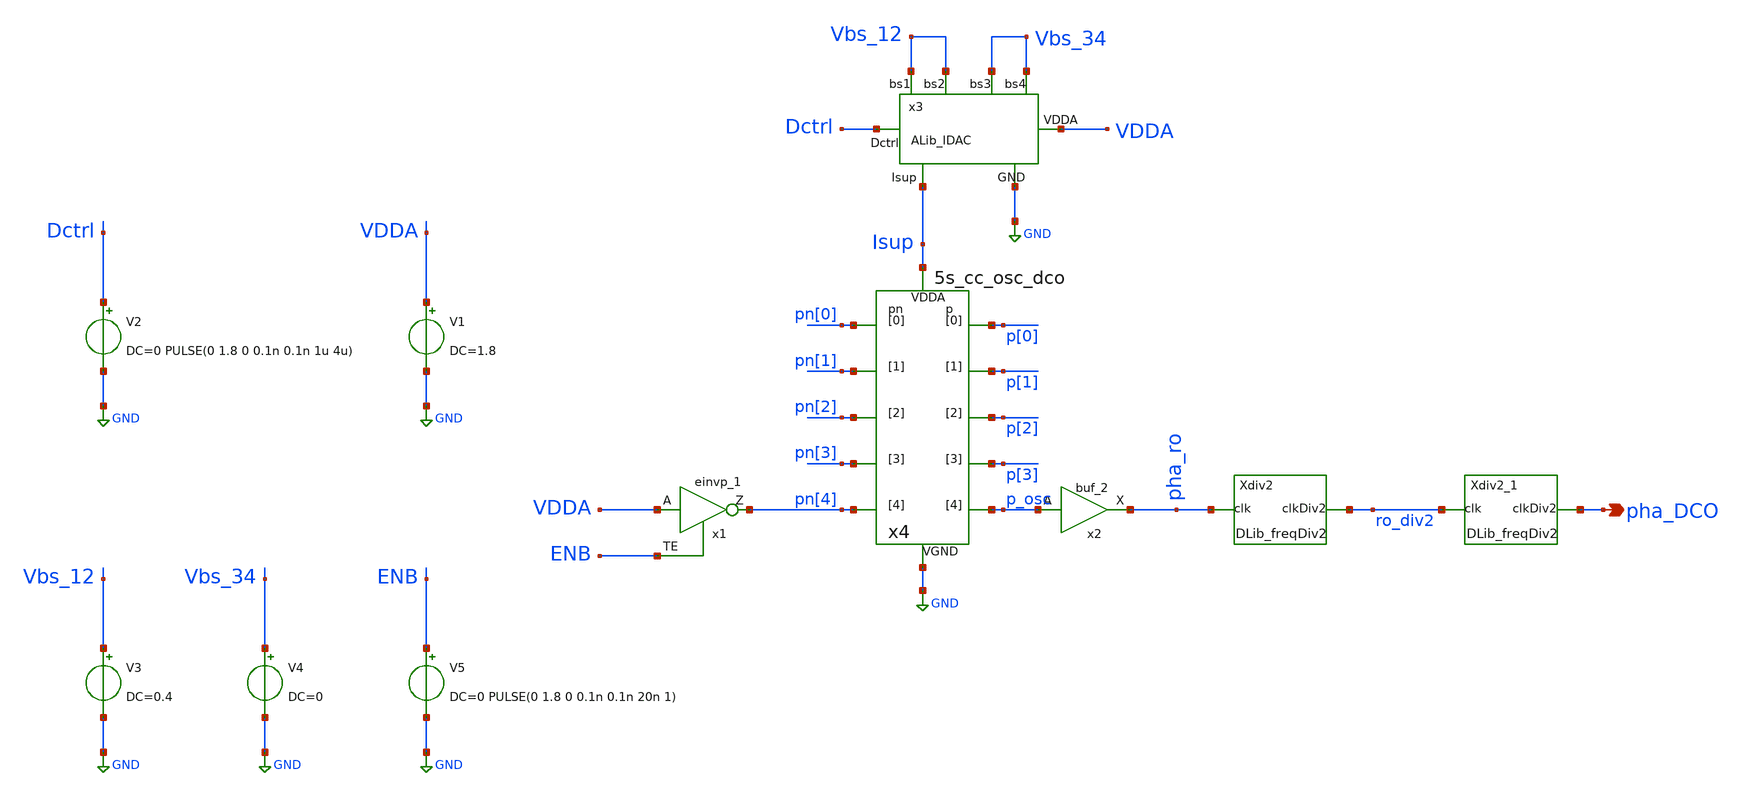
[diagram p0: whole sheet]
** sch_path: xschem/lib/ALib_DCO_tb.sch
**.subckt ALib_DCO_tb pha_DCO
*.opin pha_DCO
x1 VDDA ENB GND GND VDDA VDDA pn[4] sky130_fd_sc_hd__einvp_1
x2 p_osc GND GND VDDA VDDA pha_ro sky130_fd_sc_hd__buf_2
x3 GND VDDA Dctrl Vbs_12 Vbs_12 Vbs_34 Vbs_34 Isup ALib_IDAC
x4 GND Isup p[0] p[1] p[2] p[3] p_osc pn[0] pn[1] pn[2] pn[3] pn[4] 5s_cc_osc_dco
Xdiv2 pha_ro GND GND VDDA VDDA ro_div2 DLib_freqDiv2
Xdiv2_1 ro_div2 GND GND VCCD VCCD pha_DCO DLib_freqDiv2
V1 VDDA GND DC=1.8
V2 Dctrl GND DC=0 PULSE(0 1.8 0 0.1n 0.1n 1u 4u)
V3 Vbs_12 GND DC=0.4
V4 Vbs_34 GND DC=0
V5 ENB GND DC=0 PULSE(0 1.8 0 0.1n 0.1n 20n 1)
**** begin user architecture code


.lib /home/dkits/openpdks/sky130A/libs.tech/ngspice/sky130.lib.spice tt
.inc /home/dkits/openpdks/sky130A/libs.ref/sky130_fd_sc_hd/spice/sky130_fd_sc_hd.spice




.control
set num_threads=10
save all
TRAN 1n 50u $ start=0
.endc


**** end user architecture code
**.ends

* expanding   symbol:  ../lib/ALib_IDAC.sym # of pins=8
** sym_path: xschem/lib/ALib_IDAC.sym
** sch_path: xschem/lib/ALib_IDAC.sch
.subckt ALib_IDAC GND VDDA Dctrl Vbs1 Vbs2 Vbs3 Vbs4 Isup
*.ipin Vbs3
*.ipin Vbs4
*.ipin Vbs1
*.ipin Vbs2
*.opin Isup
*.ipin Dctrl
*.ipin GND
*.ipin VDDA
x1 open GND GND VDDA VDDA lock sky130_fd_sc_hd__inv_2
XM1 net1 Vbs1 VDDA VDDA sky130_fd_pr__pfet_01v8_hvt L=0.5 W=1.8 nf=1 ad='int((1 + 1)/2) * 1.8 / 1 * 0.29'
+ as='int((1 + 2)/2) * 1.8 / 1 * 0.29' pd='2*int((1 + 1)/2) * (1.8 / 1 + 0.29)' ps='2*int((1 + 2)/2) * (1.8 / 1 + 0.29)'
+ nrd='0.29 / 1.8 ' nrs='0.29 / 1.8 ' sa=0 sb=0 sd=0 mult=1 m=1
XM2 Isup Vbs2 net1 net1 sky130_fd_pr__pfet_01v8_hvt L=0.5 W=1.8 nf=1 ad='int((1 + 1)/2) * 1.8 / 1 * 0.29'
+ as='int((1 + 2)/2) * 1.8 / 1 * 0.29' pd='2*int((1 + 1)/2) * (1.8 / 1 + 0.29)' ps='2*int((1 + 2)/2) * (1.8 / 1 + 0.29)'
+ nrd='0.29 / 1.8 ' nrs='0.29 / 1.8 ' sa=0 sb=0 sd=0 mult=1 m=1
x2 Dctrl GND GND VDDA VDDA open sky130_fd_sc_hd__buf_2
XM3 net2 Vbs3 VDDA VDDA sky130_fd_pr__pfet_01v8_hvt L=0.5 W=5.4 nf=3 ad='int((3 + 1)/2) * 5.4 / 3 * 0.29'
+ as='int((3 + 2)/2) * 5.4 / 3 * 0.29' pd='2*int((3 + 1)/2) * (5.4 / 3 + 0.29)' ps='2*int((3 + 2)/2) * (5.4 / 3 + 0.29)'
+ nrd='0.29 / 5.4 ' nrs='0.29 / 5.4 ' sa=0 sb=0 sd=0 mult=1 m=1
XM4 add_pwr Vbs4 net2 net2 sky130_fd_pr__pfet_01v8_hvt L=0.5 W=5.4 nf=3 ad='int((3 + 1)/2) * 5.4 / 3 * 0.29'
+ as='int((3 + 2)/2) * 5.4 / 3 * 0.29' pd='2*int((3 + 1)/2) * (5.4 / 3 + 0.29)' ps='2*int((3 + 2)/2) * (5.4 / 3 + 0.29)'
+ nrd='0.29 / 5.4 ' nrs='0.29 / 5.4 ' sa=0 sb=0 sd=0 mult=1 m=1
XM5 Isup lock add_pwr add_pwr sky130_fd_pr__pfet_01v8_hvt L=0.5 W=8 nf=2 ad='int((2 + 1)/2) * 8 / 2 * 0.29'
+ as='int((2 + 2)/2) * 8 / 2 * 0.29' pd='2*int((2 + 1)/2) * (8 / 2 + 0.29)' ps='2*int((2 + 2)/2) * (8 / 2 + 0.29)'
+ nrd='0.29 / 8 ' nrs='0.29 / 8 ' sa=0 sb=0 sd=0 mult=1 m=1
XM6 add_pwr open Isup GND sky130_fd_pr__nfet_01v8 L=0.5 W=4 nf=2 ad='int((nf+1)/2) * W/nf * 0.29' as='int((nf+2)/2) * W/nf * 0.29'
+ pd='2*int((nf+1)/2) * (W/nf + 0.29)' ps='2*int((nf+2)/2) * (W/nf + 0.29)' nrd='0.29 / W' nrs='0.29 / W'
+ sa=0 sb=0 sd=0 mult=1 m=1
XM7 input_R open add_pwr add_pwr sky130_fd_pr__pfet_01v8_hvt L=0.5 W=8 nf=2 ad='int((2 + 1)/2) * 8 / 2 * 0.29'
+ as='int((2 + 2)/2) * 8 / 2 * 0.29' pd='2*int((2 + 1)/2) * (8 / 2 + 0.29)' ps='2*int((2 + 2)/2) * (8 / 2 + 0.29)'
+ nrd='0.29 / 8 ' nrs='0.29 / 8 ' sa=0 sb=0 sd=0 mult=1 m=1
XM8 add_pwr lock input_R GND sky130_fd_pr__nfet_01v8 L=0.5 W=4 nf=2 ad='int((nf+1)/2) * W/nf * 0.29'
+ as='int((nf+2)/2) * W/nf * 0.29' pd='2*int((nf+1)/2) * (W/nf + 0.29)' ps='2*int((nf+2)/2) * (W/nf + 0.29)'
+ nrd='0.29 / W' nrs='0.29 / W' sa=0 sb=0 sd=0 mult=1 m=1
XR2 GND input_R GND sky130_fd_pr__res_xhigh_po_0p35 L=8.562 mult=1 m=1
.ends


* expanding   symbol:  ../lib/5s_cc_osc_dco.sym # of pins=12
** sym_path: xschem/lib/5s_cc_osc_dco.sym
** sch_path: xschem/lib/5s_cc_osc_dco.sch
.subckt 5s_cc_osc_dco VGND VDDA p[0] p[1] p[2] p[3] p[4] pn[0] pn[1] pn[2] pn[3] pn[4]
*.iopin VDDA
*.iopin VGND
*.opin pn[0]
*.iopin p[0]
*.opin pn[1]
*.opin p[1]
*.opin p[2]
*.opin p[3]
*.opin p[4]
*.opin pn[2]
*.opin pn[3]
*.opin pn[4]
x1 VDDA p[0] p[4] pn[4] pn[0] VGND cc_inv_dco
x2 VDDA p[1] p[0] pn[0] pn[1] VGND cc_inv_dco
x3 VDDA p[2] p[1] pn[1] pn[2] VGND cc_inv_dco
x4 VDDA p[3] p[2] pn[2] pn[3] VGND cc_inv_dco
x5 VDDA p[4] p[3] pn[3] pn[4] VGND cc_inv_dco
.ends


* expanding   symbol:  ../lib/DLib_freqDiv2.sym # of pins=2
** sym_path: xschem/lib/DLib_freqDiv2.sym
** sch_path: xschem/lib/DLib_freqDiv2.sch
.subckt DLib_freqDiv2 clk VGND VNB VPB VPWR clkDiv2
*.opin clkDiv2
*.ipin clk
x1 clk D GND GND VDDA VDDA clkDiv2 Q_N sky130_fd_sc_hd__dfxbp_2
x2 clkinv Q_N_buf GND GND VDDA VDDA D sky130_fd_sc_hd__dfxtp_1
x3 clk GND GND VDDA VDDA clkinv sky130_fd_sc_hd__inv_4
x4 Q_N GND GND VDDA VDDA Q_N_buf sky130_fd_sc_hd__buf_4
.ends


* expanding   symbol:  ../lib/cc_inv_dco.sym # of pins=6
** sym_path: xschem/lib/cc_inv_dco.sym
** sch_path: xschem/lib/cc_inv_dco.sch
.subckt cc_inv_dco VDDA outp inp inn outn VGND
*.opin outp
*.ipin inn
*.iopin VGND
*.opin outn
*.ipin inp
*.iopin VDDA
x1 VDDA VGND outp inp main_inv_dco
x2 VPWR VGND outn inn main_inv_dco
x3 outp outn VDDA VGND aux_inv_dco
x4 outn outp VDDA VGND aux_inv_dco
.ends


* expanding   symbol:  ../lib/main_inv_dco.sym # of pins=4
** sym_path: xschem/lib/main_inv_dco.sym
** sch_path: xschem/lib/main_inv_dco.sch
.subckt main_inv_dco VDDA VGND Y A
*.iopin VDDA
*.iopin VGND
*.ipin A
*.opin Y
XM3 Y A VGND VGND sky130_fd_pr__nfet_01v8 L=1.2 W=4 nf=2 ad='int((nf+1)/2) * W/nf * 0.29' as='int((nf+2)/2) * W/nf * 0.29'
+ pd='2*int((nf+1)/2) * (W/nf + 0.29)' ps='2*int((nf+2)/2) * (W/nf + 0.29)' nrd='0.29 / W' nrs='0.29 / W'
+ sa=0 sb=0 sd=0 mult=1 m=1
XM2 Y A VDDA VDDA sky130_fd_pr__pfet_01v8 L=1.2 W=6 nf=2 ad='int((nf+1)/2) * W/nf * 0.29' as='int((nf+2)/2) * W/nf * 0.29'
+ pd='2*int((nf+1)/2) * (W/nf + 0.29)' ps='2*int((nf+2)/2) * (W/nf + 0.29)' nrd='0.29 / W' nrs='0.29 / W'
+ sa=0 sb=0 sd=0 mult=1 m=1
.ends


* expanding   symbol:  ../lib/aux_inv_dco.sym # of pins=4
** sym_path: xschem/lib/aux_inv_dco.sym
** sch_path: xschem/lib/aux_inv_dco.sch
.subckt aux_inv_dco A Y VDDA VGND
*.iopin VDDA
*.iopin VGND
*.ipin A
*.opin Y
XM3 Y A VGND VGND sky130_fd_pr__nfet_01v8 L=1.2 W=2 nf=1 ad='int((nf+1)/2) * W/nf * 0.29' as='int((nf+2)/2) * W/nf * 0.29'
+ pd='2*int((nf+1)/2) * (W/nf + 0.29)' ps='2*int((nf+2)/2) * (W/nf + 0.29)' nrd='0.29 / W' nrs='0.29 / W'
+ sa=0 sb=0 sd=0 mult=1 m=1
XM2 Y A VDDA VDDA sky130_fd_pr__pfet_01v8 L=1.2 W=3 nf=1 ad='int((nf+1)/2) * W/nf * 0.29' as='int((nf+2)/2) * W/nf * 0.29'
+ pd='2*int((nf+1)/2) * (W/nf + 0.29)' ps='2*int((nf+2)/2) * (W/nf + 0.29)' nrd='0.29 / W' nrs='0.29 / W'
+ sa=0 sb=0 sd=0 mult=1 m=1
.ends

.GLOBAL GND
.end
